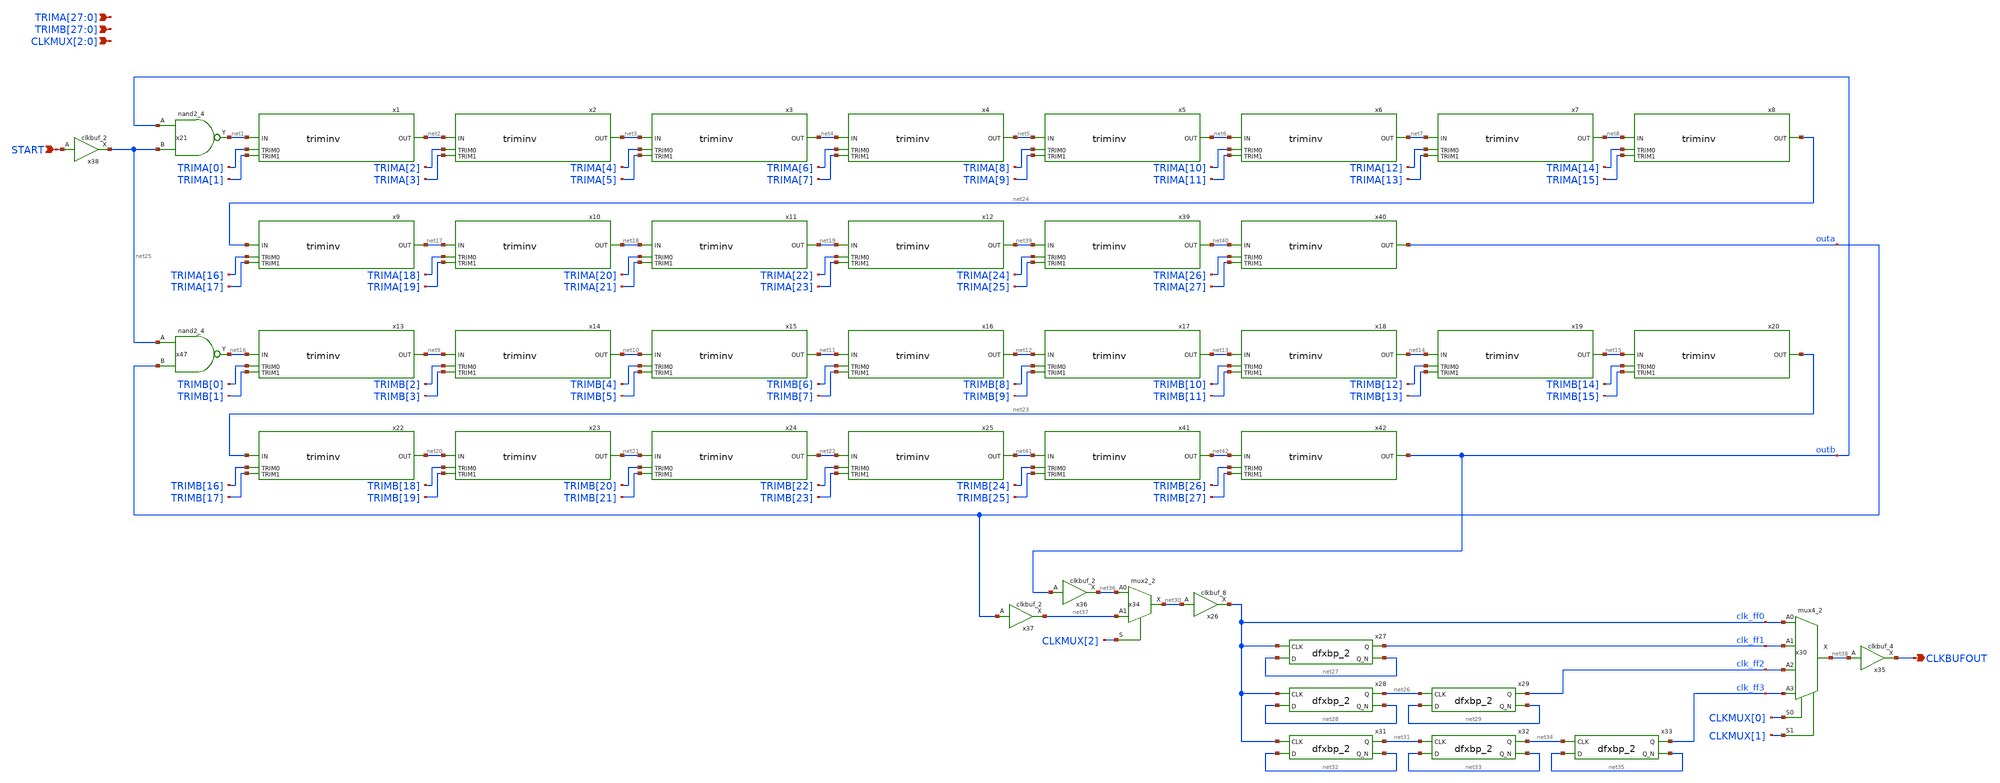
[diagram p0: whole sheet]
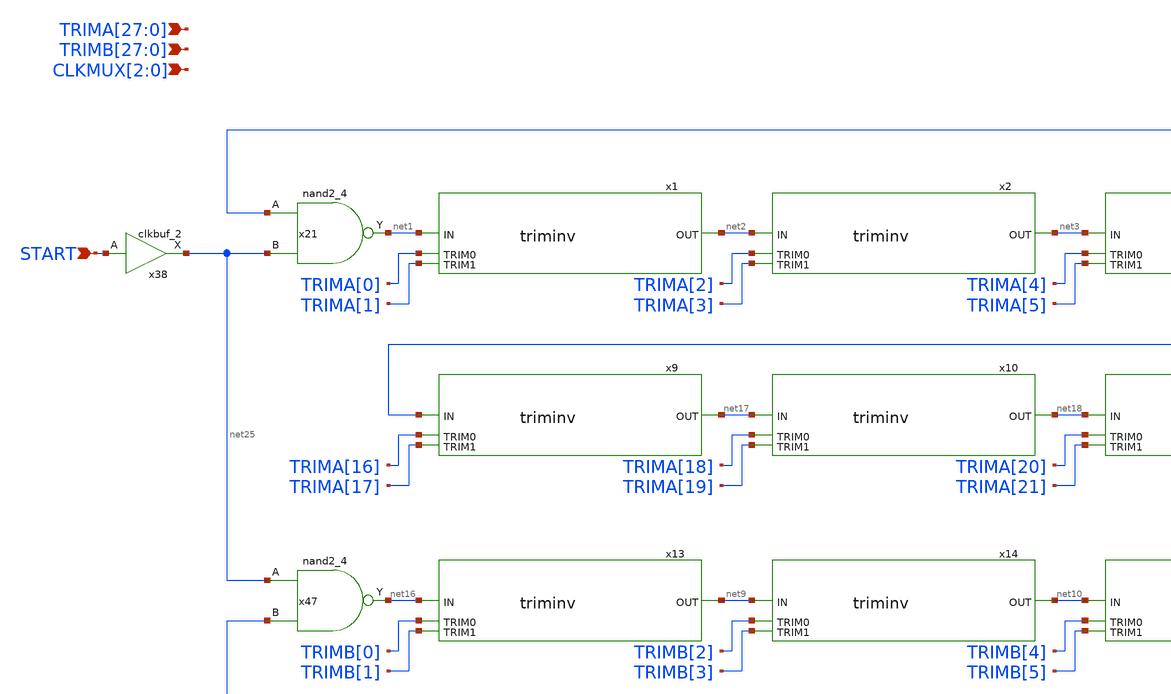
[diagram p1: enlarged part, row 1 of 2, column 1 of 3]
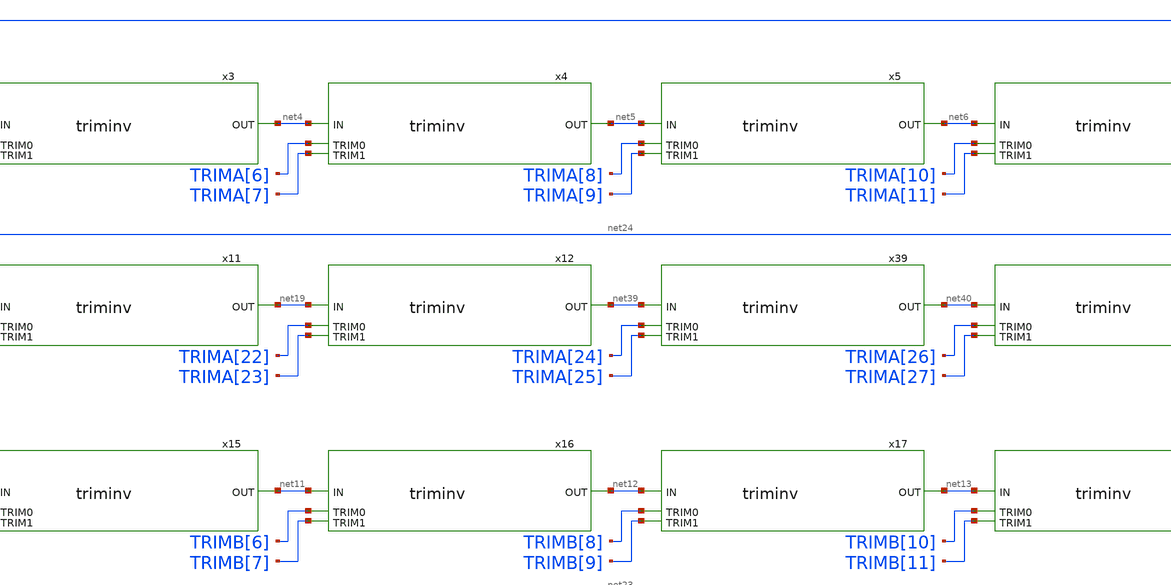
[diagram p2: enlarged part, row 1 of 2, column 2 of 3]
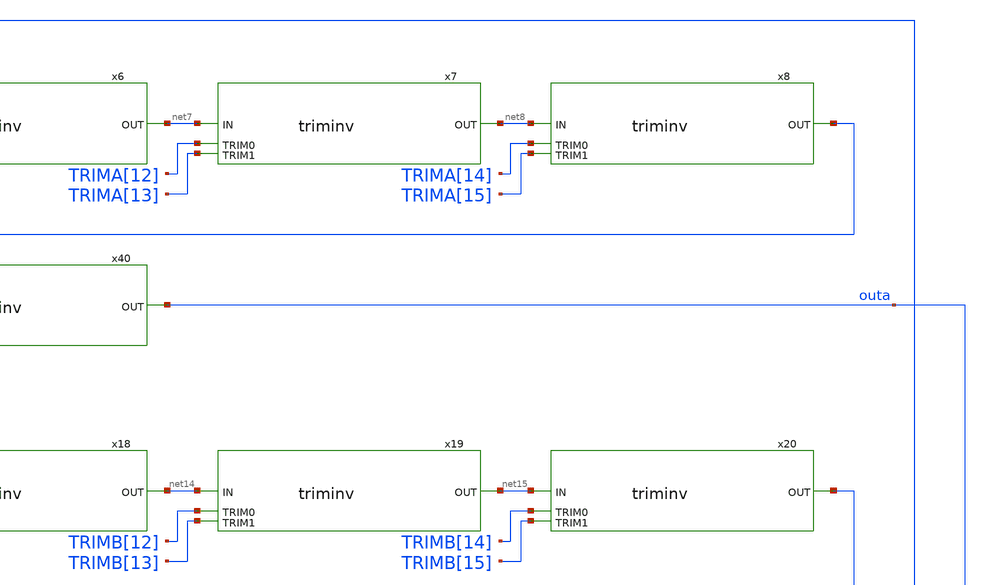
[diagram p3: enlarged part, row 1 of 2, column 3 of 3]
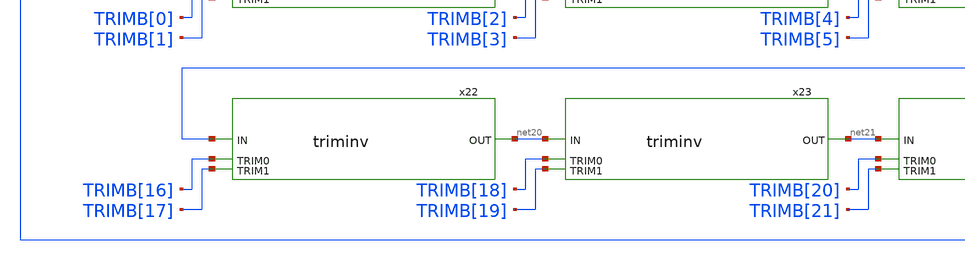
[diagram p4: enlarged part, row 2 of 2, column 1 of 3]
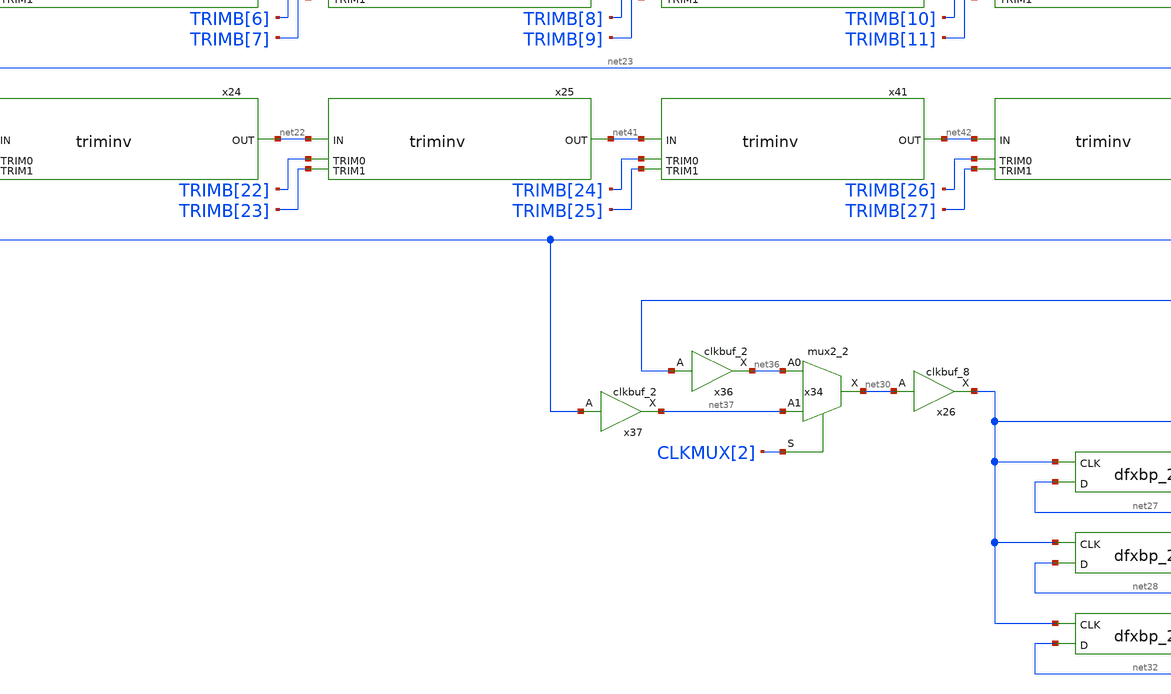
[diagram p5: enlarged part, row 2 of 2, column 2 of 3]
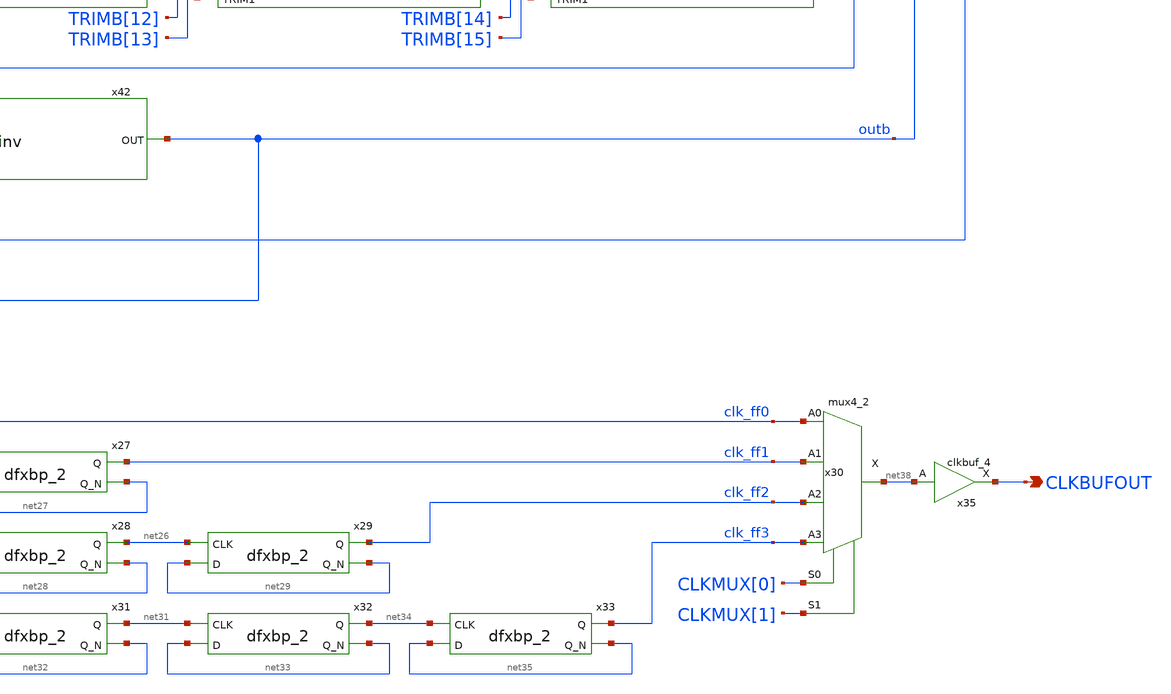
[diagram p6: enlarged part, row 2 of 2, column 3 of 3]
** sch_path: ip/randsack/sch/collapsering.sch
**.subckt collapsering CLKBUFOUT START
*+ TRIMA[27],TRIMA[26],TRIMA[25],TRIMA[24],TRIMA[23],TRIMA[22],TRIMA[21],TRIMA[20],TRIMA[19],TRIMA[18],TRIMA[17],TRIMA[16],TRIMA[15],TRIMA[14],TRIMA[13],TRIMA[12],TRIMA[11],TRIMA[10],TRIMA[9],TRIMA[8],TRIMA[7],TRIMA[6],TRIMA[5],TRIMA[4],TRIMA[3],TRIMA[2],TRIMA[1],TRIMA[0]
*+ TRIMB[27],TRIMB[26],TRIMB[25],TRIMB[24],TRIMB[23],TRIMB[22],TRIMB[21],TRIMB[20],TRIMB[19],TRIMB[18],TRIMB[17],TRIMB[16],TRIMB[15],TRIMB[14],TRIMB[13],TRIMB[12],TRIMB[11],TRIMB[10],TRIMB[9],TRIMB[8],TRIMB[7],TRIMB[6],TRIMB[5],TRIMB[4],TRIMB[3],TRIMB[2],TRIMB[1],TRIMB[0] CLKMUX[2],CLKMUX[1],CLKMUX[0]
*.opin CLKBUFOUT
*.ipin START
*.ipin
*+ TRIMA[27],TRIMA[26],TRIMA[25],TRIMA[24],TRIMA[23],TRIMA[22],TRIMA[21],TRIMA[20],TRIMA[19],TRIMA[18],TRIMA[17],TRIMA[16],TRIMA[15],TRIMA[14],TRIMA[13],TRIMA[12],TRIMA[11],TRIMA[10],TRIMA[9],TRIMA[8],TRIMA[7],TRIMA[6],TRIMA[5],TRIMA[4],TRIMA[3],TRIMA[2],TRIMA[1],TRIMA[0]
*.ipin
*+ TRIMB[27],TRIMB[26],TRIMB[25],TRIMB[24],TRIMB[23],TRIMB[22],TRIMB[21],TRIMB[20],TRIMB[19],TRIMB[18],TRIMB[17],TRIMB[16],TRIMB[15],TRIMB[14],TRIMB[13],TRIMB[12],TRIMB[11],TRIMB[10],TRIMB[9],TRIMB[8],TRIMB[7],TRIMB[6],TRIMB[5],TRIMB[4],TRIMB[3],TRIMB[2],TRIMB[1],TRIMB[0]
*.ipin CLKMUX[2],CLKMUX[1],CLKMUX[0]
x21 outb net25 VGND VNB VPB VPWR net1 sky130_fd_sc_hd__nand2_4
x47 net25 outa VGND VNB VPB VPWR net16 sky130_fd_sc_hd__nand2_4
x35 net38 VGND VNB VPB VPWR CLKBUFOUT sky130_fd_sc_hd__clkbuf_4
x1 net2 net1 TRIMA[0] TRIMA[1] triminv
x2 net3 net2 TRIMA[2] TRIMA[3] triminv
x3 net4 net3 TRIMA[4] TRIMA[5] triminv
x4 net5 net4 TRIMA[6] TRIMA[7] triminv
x5 net6 net5 TRIMA[8] TRIMA[9] triminv
x6 net7 net6 TRIMA[10] TRIMA[11] triminv
x7 net8 net7 TRIMA[12] TRIMA[13] triminv
x8 net24 net8 TRIMA[14] TRIMA[15] triminv
x9 net17 net24 TRIMA[16] TRIMA[17] triminv
x10 net18 net17 TRIMA[18] TRIMA[19] triminv
x11 net19 net18 TRIMA[20] TRIMA[21] triminv
x12 net39 net19 TRIMA[22] TRIMA[23] triminv
x13 net9 net16 TRIMB[0] TRIMB[1] triminv
x14 net10 net9 TRIMB[2] TRIMB[3] triminv
x15 net11 net10 TRIMB[4] TRIMB[5] triminv
x16 net12 net11 TRIMB[6] TRIMB[7] triminv
x17 net13 net12 TRIMB[8] TRIMB[9] triminv
x18 net14 net13 TRIMB[10] TRIMB[11] triminv
x19 net15 net14 TRIMB[12] TRIMB[13] triminv
x20 net23 net15 TRIMB[14] TRIMB[15] triminv
x22 net20 net23 TRIMB[16] TRIMB[17] triminv
x23 net21 net20 TRIMB[18] TRIMB[19] triminv
x24 net22 net21 TRIMB[20] TRIMB[21] triminv
x25 net41 net22 TRIMB[22] TRIMB[23] triminv
x27 clk_ff0 net27 VGND VNB VPB VPWR clk_ff1 net27 sky130_fd_sc_hd__dfxbp_2
x28 clk_ff0 net28 VGND VNB VPB VPWR net26 net28 sky130_fd_sc_hd__dfxbp_2
x29 net26 net29 VGND VNB VPB VPWR clk_ff2 net29 sky130_fd_sc_hd__dfxbp_2
x26 net30 VGND VNB VPB VPWR clk_ff0 sky130_fd_sc_hd__clkbuf_8
x30 clk_ff0 clk_ff1 clk_ff2 clk_ff3 CLKMUX[0] CLKMUX[1] VGND VNB VPB VPWR net38
+ sky130_fd_sc_hd__mux4_2
x31 clk_ff0 net32 VGND VNB VPB VPWR net31 net32 sky130_fd_sc_hd__dfxbp_2
x32 net31 net33 VGND VNB VPB VPWR net34 net33 sky130_fd_sc_hd__dfxbp_2
x33 net34 net35 VGND VNB VPB VPWR clk_ff3 net35 sky130_fd_sc_hd__dfxbp_2
x34 net36 net37 CLKMUX[2] VGND VNB VPB VPWR net30 sky130_fd_sc_hd__mux2_2
x36 outb VGND VNB VPB VPWR net36 sky130_fd_sc_hd__clkbuf_2
x37 outa VGND VNB VPB VPWR net37 sky130_fd_sc_hd__clkbuf_2
x38 START VGND VNB VPB VPWR net25 sky130_fd_sc_hd__clkbuf_2
x39 net40 net39 TRIMA[24] TRIMA[25] triminv
x40 outa net40 TRIMA[26] TRIMA[27] triminv
x41 net42 net41 TRIMB[24] TRIMB[25] triminv
x42 outb net42 TRIMB[26] TRIMB[27] triminv
**.ends

* expanding   symbol:  /home/harrison/workspace/randsack/ip/randsack/sch/triminv.sym # of pins=4
** sym_path: ip/randsack/sch/triminv.sym
** sch_path: ip/randsack/sch/triminv.sch
.subckt triminv OUT IN TRIM0 TRIM1
*.ipin IN
*.ipin OUT
*.ipin TRIM0
*.ipin TRIM1
x1 IN VGND VNB VPB VPWR ts sky130_fd_sc_hd__clkbuf_2
x2 ts TRIM1 VGND VNB VPB VPWR d1 sky130_fd_sc_hd__einvn_4
x3 d1 VGND VNB VPB VPWR d2 sky130_fd_sc_hd__clkinv_1
x4 d2 TRIM0 VGND VNB VPB VPWR OUT sky130_fd_sc_hd__einvp_2
x5 ts VGND VNB VPB VPWR d0 sky130_fd_sc_hd__clkbuf_1
x6 d0 TRIM1 VGND VNB VPB VPWR d1 sky130_fd_sc_hd__einvp_2
x7 ts TRIM0 VGND VNB VPB VPWR OUT sky130_fd_sc_hd__einvn_8
.ends

.end
